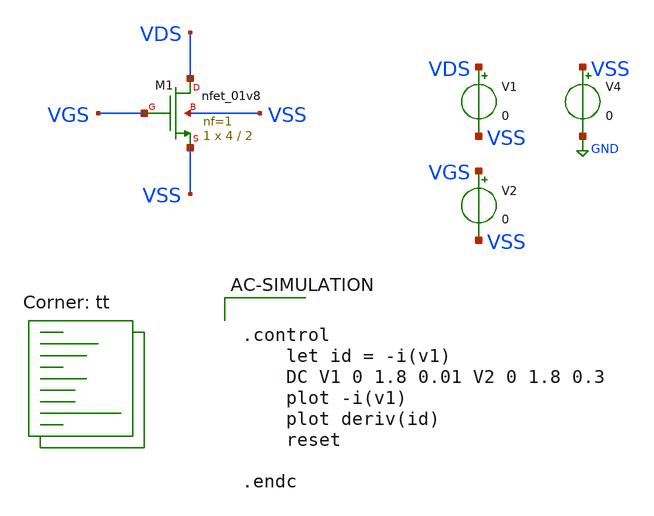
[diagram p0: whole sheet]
** sch_path: designs/libs/core_analog/p-ota/tb_nmos.sch
**.subckt tb_nmos
XM1 VDS VGS VSS VSS sky130_fd_pr__nfet_01v8 L=2 W=4 nf=1 ad='int((nf+1)/2) * W/nf * 0.29' as='int((nf+2)/2) * W/nf * 0.29'
+ pd='2*int((nf+1)/2) * (W/nf + 0.29)' ps='2*int((nf+2)/2) * (W/nf + 0.29)' nrd='0.29 / W' nrs='0.29 / W'
+ sa=0 sb=0 sd=0 mult=1 m=1
V1 VDS VSS 0
V4 VSS GND 0
V2 VGS VSS 0
**** begin user architecture code
.lib $::SKYWATER_MODELS/sky130.lib.spice tt


.control
	let id = -i(v1)
	DC V1 0 1.8 0.01 V2 0 1.8 0.3
	plot -i(v1)
	plot deriv(id)
	reset

.endc

**** end user architecture code
**.ends
.GLOBAL GND
.end
